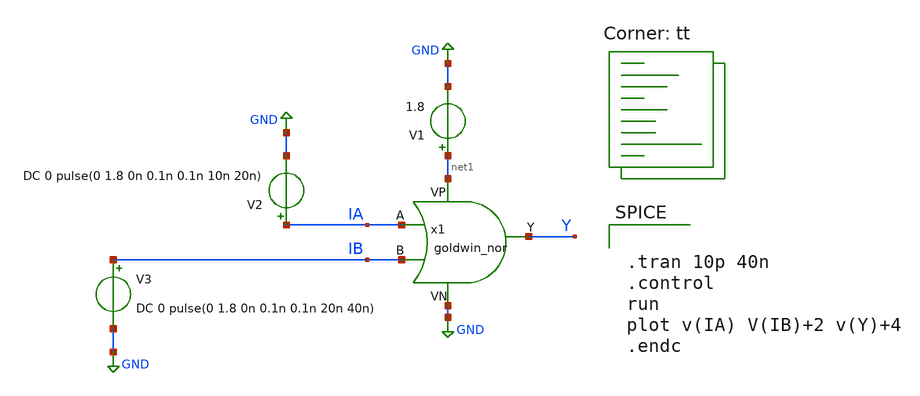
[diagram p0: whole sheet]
** sch_path: APIC-UTS/schematic/goldwin_nor/tb_goldwin_nor.sch
**.subckt tb_goldwin_nor
V1 net1 GND 1.8
V2 IA GND DC 0 pulse(0 1.8 0n 0.1n 0.1n 10n 20n)
V3 IB GND DC 0 pulse(0 1.8 0n 0.1n 0.1n 20n 40n)
x1 IA IB Y net1 GND goldwin_nor
**** begin user architecture code


.tran 10p 40n
.control
run
plot v(IA) V(IB)+2 v(Y)+4
.endc


.lib $::SKYWATER_MODELS/sky130.lib.spice tt
**** end user architecture code
**.ends

* expanding   symbol:  goldwin_nor.sym # of pins=5
** sym_path: APIC-UTS/schematic/goldwin_nor/goldwin_nor.sym
** sch_path: APIC-UTS/schematic/goldwin_nor/goldwin_nor.sch
.subckt goldwin_nor A B Y VP VN
*.ipin A
*.ipin B
*.ipin VP
*.ipin VN
*.opin Y
XM1 net1 A VP VP sky130_fd_pr__pfet_01v8 L=0.15 W=3 nf=1 ad='int((nf+1)/2) * W/nf * 0.29' as='int((nf+2)/2) * W/nf * 0.29'
+ pd='2*int((nf+1)/2) * (W/nf + 0.29)' ps='2*int((nf+2)/2) * (W/nf + 0.29)' nrd='0.29 / W' nrs='0.29 / W'
+ sa=0 sb=0 sd=0 mult=1 m=1
XM2 Y B net1 VP sky130_fd_pr__pfet_01v8 L=0.15 W=3 nf=1 ad='int((nf+1)/2) * W/nf * 0.29' as='int((nf+2)/2) * W/nf * 0.29'
+ pd='2*int((nf+1)/2) * (W/nf + 0.29)' ps='2*int((nf+2)/2) * (W/nf + 0.29)' nrd='0.29 / W' nrs='0.29 / W'
+ sa=0 sb=0 sd=0 mult=1 m=1
XM3 Y B VN VN sky130_fd_pr__nfet_01v8 L=0.15 W=1 nf=1 ad='int((nf+1)/2) * W/nf * 0.29' as='int((nf+2)/2) * W/nf * 0.29'
+ pd='2*int((nf+1)/2) * (W/nf + 0.29)' ps='2*int((nf+2)/2) * (W/nf + 0.29)' nrd='0.29 / W' nrs='0.29 / W'
+ sa=0 sb=0 sd=0 mult=1 m=1
XM4 Y A VN VN sky130_fd_pr__nfet_01v8 L=0.15 W=1 nf=1 ad='int((nf+1)/2) * W/nf * 0.29' as='int((nf+2)/2) * W/nf * 0.29'
+ pd='2*int((nf+1)/2) * (W/nf + 0.29)' ps='2*int((nf+2)/2) * (W/nf + 0.29)' nrd='0.29 / W' nrs='0.29 / W'
+ sa=0 sb=0 sd=0 mult=1 m=1
.ends

.GLOBAL GND
.end
